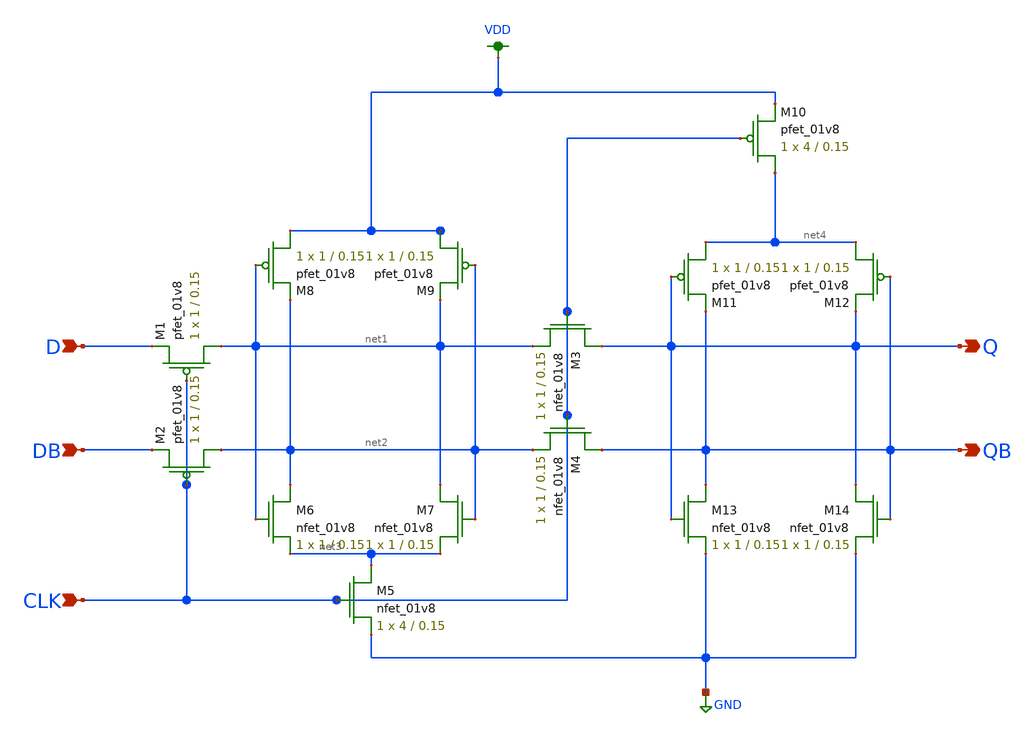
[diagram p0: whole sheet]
** sch_path: schemas/DFF.sch
**.subckt DFF D DB CLK Q QB
*.ipin D
*.ipin DB
*.ipin CLK
*.opin Q
*.opin QB
XM1 net1 CLK D VDD sky130_fd_pr__pfet_01v8 L=0.15 W=1 nf=1 ad='int((nf+1)/2) * W/nf * 0.29' as='int((nf+2)/2) * W/nf * 0.29'
+ pd='2*int((nf+1)/2) * (W/nf + 0.29)' ps='2*int((nf+2)/2) * (W/nf + 0.29)' nrd='0.29 / W' nrs='0.29 / W'
+ sa=0 sb=0 sd=0 mult=1 m=1
XM2 net2 CLK DB VDD sky130_fd_pr__pfet_01v8 L=0.15 W=1 nf=1 ad='int((nf+1)/2) * W/nf * 0.29' as='int((nf+2)/2) * W/nf * 0.29'
+ pd='2*int((nf+1)/2) * (W/nf + 0.29)' ps='2*int((nf+2)/2) * (W/nf + 0.29)' nrd='0.29 / W' nrs='0.29 / W'
+ sa=0 sb=0 sd=0 mult=1 m=1
XM3 Q CLK net1 GND sky130_fd_pr__nfet_01v8 L=0.15 W=1 nf=1 ad='int((nf+1)/2) * W/nf * 0.29' as='int((nf+2)/2) * W/nf * 0.29'
+ pd='2*int((nf+1)/2) * (W/nf + 0.29)' ps='2*int((nf+2)/2) * (W/nf + 0.29)' nrd='0.29 / W' nrs='0.29 / W'
+ sa=0 sb=0 sd=0 mult=1 m=1
XM4 QB CLK net2 GND sky130_fd_pr__nfet_01v8 L=0.15 W=1 nf=1 ad='int((nf+1)/2) * W/nf * 0.29' as='int((nf+2)/2) * W/nf * 0.29'
+ pd='2*int((nf+1)/2) * (W/nf + 0.29)' ps='2*int((nf+2)/2) * (W/nf + 0.29)' nrd='0.29 / W' nrs='0.29 / W'
+ sa=0 sb=0 sd=0 mult=1 m=1
XM5 net3 CLK GND GND sky130_fd_pr__nfet_01v8 L=0.15 W=4 nf=1 ad='int((nf+1)/2) * W/nf * 0.29' as='int((nf+2)/2) * W/nf * 0.29'
+ pd='2*int((nf+1)/2) * (W/nf + 0.29)' ps='2*int((nf+2)/2) * (W/nf + 0.29)' nrd='0.29 / W' nrs='0.29 / W'
+ sa=0 sb=0 sd=0 mult=1 m=1
XM6 net2 net1 net3 GND sky130_fd_pr__nfet_01v8 L=0.15 W=1 nf=1 ad='int((nf+1)/2) * W/nf * 0.29' as='int((nf+2)/2) * W/nf * 0.29'
+ pd='2*int((nf+1)/2) * (W/nf + 0.29)' ps='2*int((nf+2)/2) * (W/nf + 0.29)' nrd='0.29 / W' nrs='0.29 / W'
+ sa=0 sb=0 sd=0 mult=1 m=1
XM7 net1 net2 net3 GND sky130_fd_pr__nfet_01v8 L=0.15 W=1 nf=1 ad='int((nf+1)/2) * W/nf * 0.29' as='int((nf+2)/2) * W/nf * 0.29'
+ pd='2*int((nf+1)/2) * (W/nf + 0.29)' ps='2*int((nf+2)/2) * (W/nf + 0.29)' nrd='0.29 / W' nrs='0.29 / W'
+ sa=0 sb=0 sd=0 mult=1 m=1
XM8 VDD net1 net2 VDD sky130_fd_pr__pfet_01v8 L=0.15 W=1 nf=1 ad='int((nf+1)/2) * W/nf * 0.29' as='int((nf+2)/2) * W/nf * 0.29'
+ pd='2*int((nf+1)/2) * (W/nf + 0.29)' ps='2*int((nf+2)/2) * (W/nf + 0.29)' nrd='0.29 / W' nrs='0.29 / W'
+ sa=0 sb=0 sd=0 mult=1 m=1
XM9 VDD net2 net1 VDD sky130_fd_pr__pfet_01v8 L=0.15 W=1 nf=1 ad='int((nf+1)/2) * W/nf * 0.29' as='int((nf+2)/2) * W/nf * 0.29'
+ pd='2*int((nf+1)/2) * (W/nf + 0.29)' ps='2*int((nf+2)/2) * (W/nf + 0.29)' nrd='0.29 / W' nrs='0.29 / W'
+ sa=0 sb=0 sd=0 mult=1 m=1
XM10 net4 CLK VDD VDD sky130_fd_pr__pfet_01v8 L=0.15 W=4 nf=1 ad='int((nf+1)/2) * W/nf * 0.29' as='int((nf+2)/2) * W/nf * 0.29'
+ pd='2*int((nf+1)/2) * (W/nf + 0.29)' ps='2*int((nf+2)/2) * (W/nf + 0.29)' nrd='0.29 / W' nrs='0.29 / W'
+ sa=0 sb=0 sd=0 mult=1 m=1
XM11 net4 Q QB VDD sky130_fd_pr__pfet_01v8 L=0.15 W=1 nf=1 ad='int((nf+1)/2) * W/nf * 0.29' as='int((nf+2)/2) * W/nf * 0.29'
+ pd='2*int((nf+1)/2) * (W/nf + 0.29)' ps='2*int((nf+2)/2) * (W/nf + 0.29)' nrd='0.29 / W' nrs='0.29 / W'
+ sa=0 sb=0 sd=0 mult=1 m=1
XM12 net4 QB Q VDD sky130_fd_pr__pfet_01v8 L=0.15 W=1 nf=1 ad='int((nf+1)/2) * W/nf * 0.29' as='int((nf+2)/2) * W/nf * 0.29'
+ pd='2*int((nf+1)/2) * (W/nf + 0.29)' ps='2*int((nf+2)/2) * (W/nf + 0.29)' nrd='0.29 / W' nrs='0.29 / W'
+ sa=0 sb=0 sd=0 mult=1 m=1
XM13 QB Q GND GND sky130_fd_pr__nfet_01v8 L=0.15 W=1 nf=1 ad='int((nf+1)/2) * W/nf * 0.29' as='int((nf+2)/2) * W/nf * 0.29'
+ pd='2*int((nf+1)/2) * (W/nf + 0.29)' ps='2*int((nf+2)/2) * (W/nf + 0.29)' nrd='0.29 / W' nrs='0.29 / W'
+ sa=0 sb=0 sd=0 mult=1 m=1
XM14 Q QB GND GND sky130_fd_pr__nfet_01v8 L=0.15 W=1 nf=1 ad='int((nf+1)/2) * W/nf * 0.29' as='int((nf+2)/2) * W/nf * 0.29'
+ pd='2*int((nf+1)/2) * (W/nf + 0.29)' ps='2*int((nf+2)/2) * (W/nf + 0.29)' nrd='0.29 / W' nrs='0.29 / W'
+ sa=0 sb=0 sd=0 mult=1 m=1
**.ends
.GLOBAL VDD
.GLOBAL GND
.end
